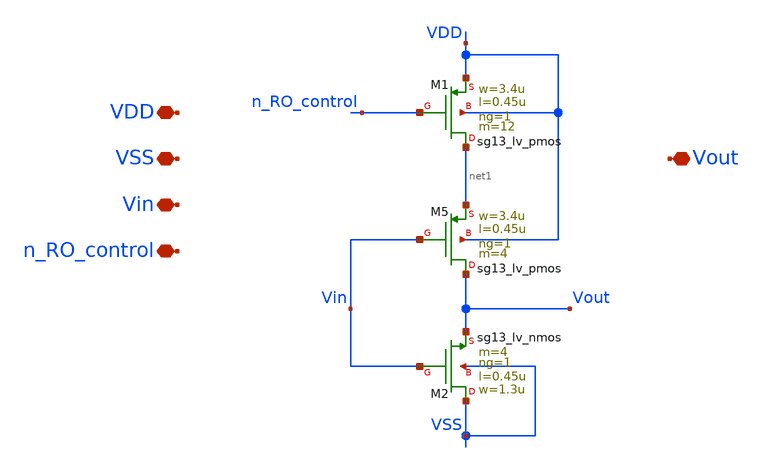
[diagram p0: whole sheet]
** sch_path: unic_cass_wrapper_user_project/ROs_reliability/inv1.sch
**.subckt inv1 VDD VSS Vin Vout n_RO_control
*.iopin VDD
*.iopin VSS
*.iopin Vin
*.iopin Vout
*.iopin n_RO_control
XM1 net1 n_RO_control VDD VDD sg13_lv_pmos w=3.4u l=0.45u ng=1 m=12 mm_ok=1
XM5 Vout Vin net1 VDD sg13_lv_pmos w=3.4u l=0.45u ng=1 m=4 mm_ok=1
XM2 VSS Vin Vout VSS sg13_lv_nmos w=1.3u l=0.45u ng=1 m=4 mm_ok=1
**.ends
.end
